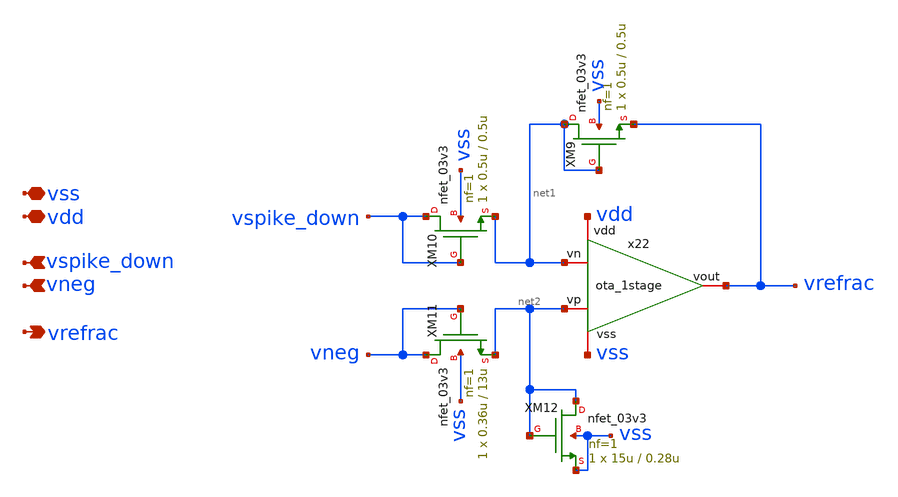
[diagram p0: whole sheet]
** sch_path: designs/libs/core_LIF_comp/core_refractory/refractory.sch
**.subckt refractory vspike_down vdd vss vrefrac vneg
*.ipin vspike_down
*.iopin vdd
*.iopin vss
*.opin vrefrac
*.ipin vneg
x22 vdd vrefrac net2 net1 vss ota_1stage
XM9 net1 net1 vrefrac vss nfet_03v3 L=0.5u W=0.5u nf=1 ad='int((nf+1)/2) * W/nf * 0.18u' as='int((nf+2)/2) * W/nf * 0.18u'
+ pd='2*int((nf+1)/2) * (W/nf + 0.18u)' ps='2*int((nf+2)/2) * (W/nf + 0.18u)' nrd='0.18u / W' nrs='0.18u / W'
+ sa=0 sb=0 sd=0 m=1
XM10 vspike_down vspike_down net1 vss nfet_03v3 L=0.5u W=0.5u nf=1 ad='int((nf+1)/2) * W/nf * 0.18u'
+ as='int((nf+2)/2) * W/nf * 0.18u' pd='2*int((nf+1)/2) * (W/nf + 0.18u)' ps='2*int((nf+2)/2) * (W/nf + 0.18u)'
+ nrd='0.18u / W' nrs='0.18u / W' sa=0 sb=0 sd=0 m=1
XM11 vneg vneg net2 vss nfet_03v3 L=13u W=0.36u nf=1 ad='int((nf+1)/2) * W/nf * 0.18u' as='int((nf+2)/2) * W/nf * 0.18u'
+ pd='2*int((nf+1)/2) * (W/nf + 0.18u)' ps='2*int((nf+2)/2) * (W/nf + 0.18u)' nrd='0.18u / W' nrs='0.18u / W'
+ sa=0 sb=0 sd=0 m=1
XM12 net2 net2 vss vss nfet_03v3 L=0.28u W=15u nf=1 ad='int((nf+1)/2) * W/nf * 0.18u' as='int((nf+2)/2) * W/nf * 0.18u'
+ pd='2*int((nf+1)/2) * (W/nf + 0.18u)' ps='2*int((nf+2)/2) * (W/nf + 0.18u)' nrd='0.18u / W' nrs='0.18u / W'
+ sa=0 sb=0 sd=0 m=1
**.ends

* expanding   symbol:  designs/libs/core_LIF_comp/core_ota_1stage/ota_1stage.sym # of pins=5
** sym_path: designs/libs/core_LIF_comp/core_ota_1stage/ota_1stage.sym
** sch_path: designs/libs/core_LIF_comp/core_ota_1stage/ota_1stage.sch
.subckt ota_1stage vdd vout vp vn vss
*.iopin vdd
*.iopin vss
*.iopin vp
*.iopin vn
*.iopin vout
XM1 net1 net1 vdd vdd pfet_03v3 L=0.28u W=0.84u nf=1 ad='int((nf+1)/2) * W/nf * 0.18u' as='int((nf+2)/2) * W/nf * 0.18u'
+ pd='2*int((nf+1)/2) * (W/nf + 0.18u)' ps='2*int((nf+2)/2) * (W/nf + 0.18u)' nrd='0.18u / W' nrs='0.18u / W'
+ sa=0 sb=0 sd=0 m=1
XM2 net1 vp net2 vss nfet_03v3 L=0.28u W=3.08u nf=1 ad='int((nf+1)/2) * W/nf * 0.18u' as='int((nf+2)/2) * W/nf * 0.18u'
+ pd='2*int((nf+1)/2) * (W/nf + 0.18u)' ps='2*int((nf+2)/2) * (W/nf + 0.18u)' nrd='0.18u / W' nrs='0.18u / W'
+ sa=0 sb=0 sd=0 m=1
XM4 vout net1 vdd vdd pfet_03v3 L=0.28u W=0.84u nf=1 ad='int((nf+1)/2) * W/nf * 0.18u' as='int((nf+2)/2) * W/nf * 0.18u'
+ pd='2*int((nf+1)/2) * (W/nf + 0.18u)' ps='2*int((nf+2)/2) * (W/nf + 0.18u)' nrd='0.18u / W' nrs='0.18u / W'
+ sa=0 sb=0 sd=0 m=1
XM3 vout vn net2 vss nfet_03v3 L=0.28u W=3.08u nf=1 ad='int((nf+1)/2) * W/nf * 0.18u' as='int((nf+2)/2) * W/nf * 0.18u'
+ pd='2*int((nf+1)/2) * (W/nf + 0.18u)' ps='2*int((nf+2)/2) * (W/nf + 0.18u)' nrd='0.18u / W' nrs='0.18u / W'
+ sa=0 sb=0 sd=0 m=1
XM5 net2 net3 vss vss nfet_03v3 L=0.28u W=0.84u nf=1 ad='int((nf+1)/2) * W/nf * 0.18u' as='int((nf+2)/2) * W/nf * 0.18u'
+ pd='2*int((nf+1)/2) * (W/nf + 0.18u)' ps='2*int((nf+2)/2) * (W/nf + 0.18u)' nrd='0.18u / W' nrs='0.18u / W'
+ sa=0 sb=0 sd=0 m=1
XM6 net3 net3 vss vss nfet_03v3 L=0.28u W=0.84u nf=1 ad='int((nf+1)/2) * W/nf * 0.18u' as='int((nf+2)/2) * W/nf * 0.18u'
+ pd='2*int((nf+1)/2) * (W/nf + 0.18u)' ps='2*int((nf+2)/2) * (W/nf + 0.18u)' nrd='0.18u / W' nrs='0.18u / W'
+ sa=0 sb=0 sd=0 m=1
XM7 vdd vdd net3 vss nfet_03v3 L=8.54u W=0.28u nf=1 ad='int((nf+1)/2) * W/nf * 0.18u' as='int((nf+2)/2) * W/nf * 0.18u'
+ pd='2*int((nf+1)/2) * (W/nf + 0.18u)' ps='2*int((nf+2)/2) * (W/nf + 0.18u)' nrd='0.18u / W' nrs='0.18u / W'
+ sa=0 sb=0 sd=0 m=1
.ends

.end
